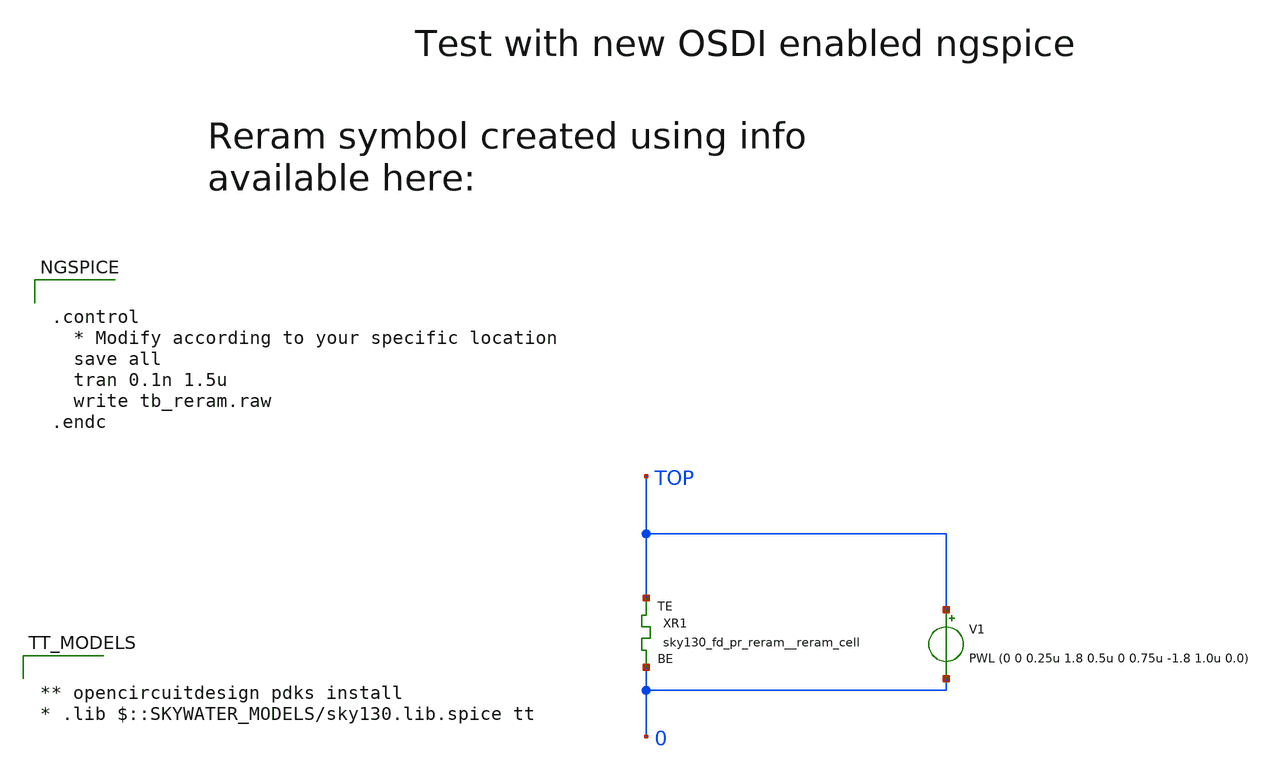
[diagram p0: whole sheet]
** sch_path: sky130_tests/tb_reram.sch
* Copyright 2021 Stefan Frederik Schippers
* Licensed under the Apache License, Version 2.0 (the "License");
* you may not use this file except in compliance with the License.
* You may obtain a copy of the License at
* https://www.apache.org/licenses/LICENSE-2.0
* Unless required by applicable law or agreed to in writing, software
* distributed under the License is distributed on an "AS IS" BASIS,
* WITHOUT WARRANTIES OR CONDITIONS OF ANY KIND, either express or implied.
* See the License for the specific language governing permissions and
* limitations under the License.
**.subckt tb_reram
V1 TOP 0 PWL (0 0 0.25u 1.8 0.5u 0 0.75u -1.8 1.0u 0.0)
XR1 TOP 0 sky130_fd_pr_reram__reram_cell Tfilament_0=3.8e-9
**** begin user architecture code


.control
  * Modify according to your specific location
  save all
  tran 0.1n 1.5u
  write tb_reram.raw
.endc




** opencircuitdesign pdks install
* .lib $::SKYWATER_MODELS/sky130.lib.spice tt

**** end user architecture code
**.ends
**** begin user architecture code

.subckt sky130_fd_pr_reram__reram_cell TE BE Tfilament_0=3.3e-9 area_ox=0.1024e-12
N1 TE BE nFilament sky130_fd_pr_reram__reram_model
.ic v(nFilament)={Tfilament_0*1.0e9}
.ends sky130_fd_pr_reram__reram_cell

.model sky130_fd_pr_reram__reram_model sky130_fd_pr_reram__reram_module area_ox=0.1024e-12  area_ox
+ = 0.1024e-12  Tox = 5.0  Tfilament_max = 4.9  Tfilament_min = 3.3  Eact_generation = 1.501
+  Eact_recombination  = 1.500  I_k1  = 6.140e-5  Tfilament_ref = 4.7249  V_ref = 0.430  velocity_k1 = 150  gamma_k0  =
+ 16.5  gamma_k1  = -1.25  Temperature_0 = 300  C_thermal = 3.1825e-16  tau_thermal = 0.23e-9  t_step  =
+ 1.0e-9  smoothing = 1e-7  Kclip = 200

.control
pre_osdi $SKYWATER_MODELS/sky130_fd_pr_reram__reram_module.osdi
.endc

**** end user architecture code
.end
